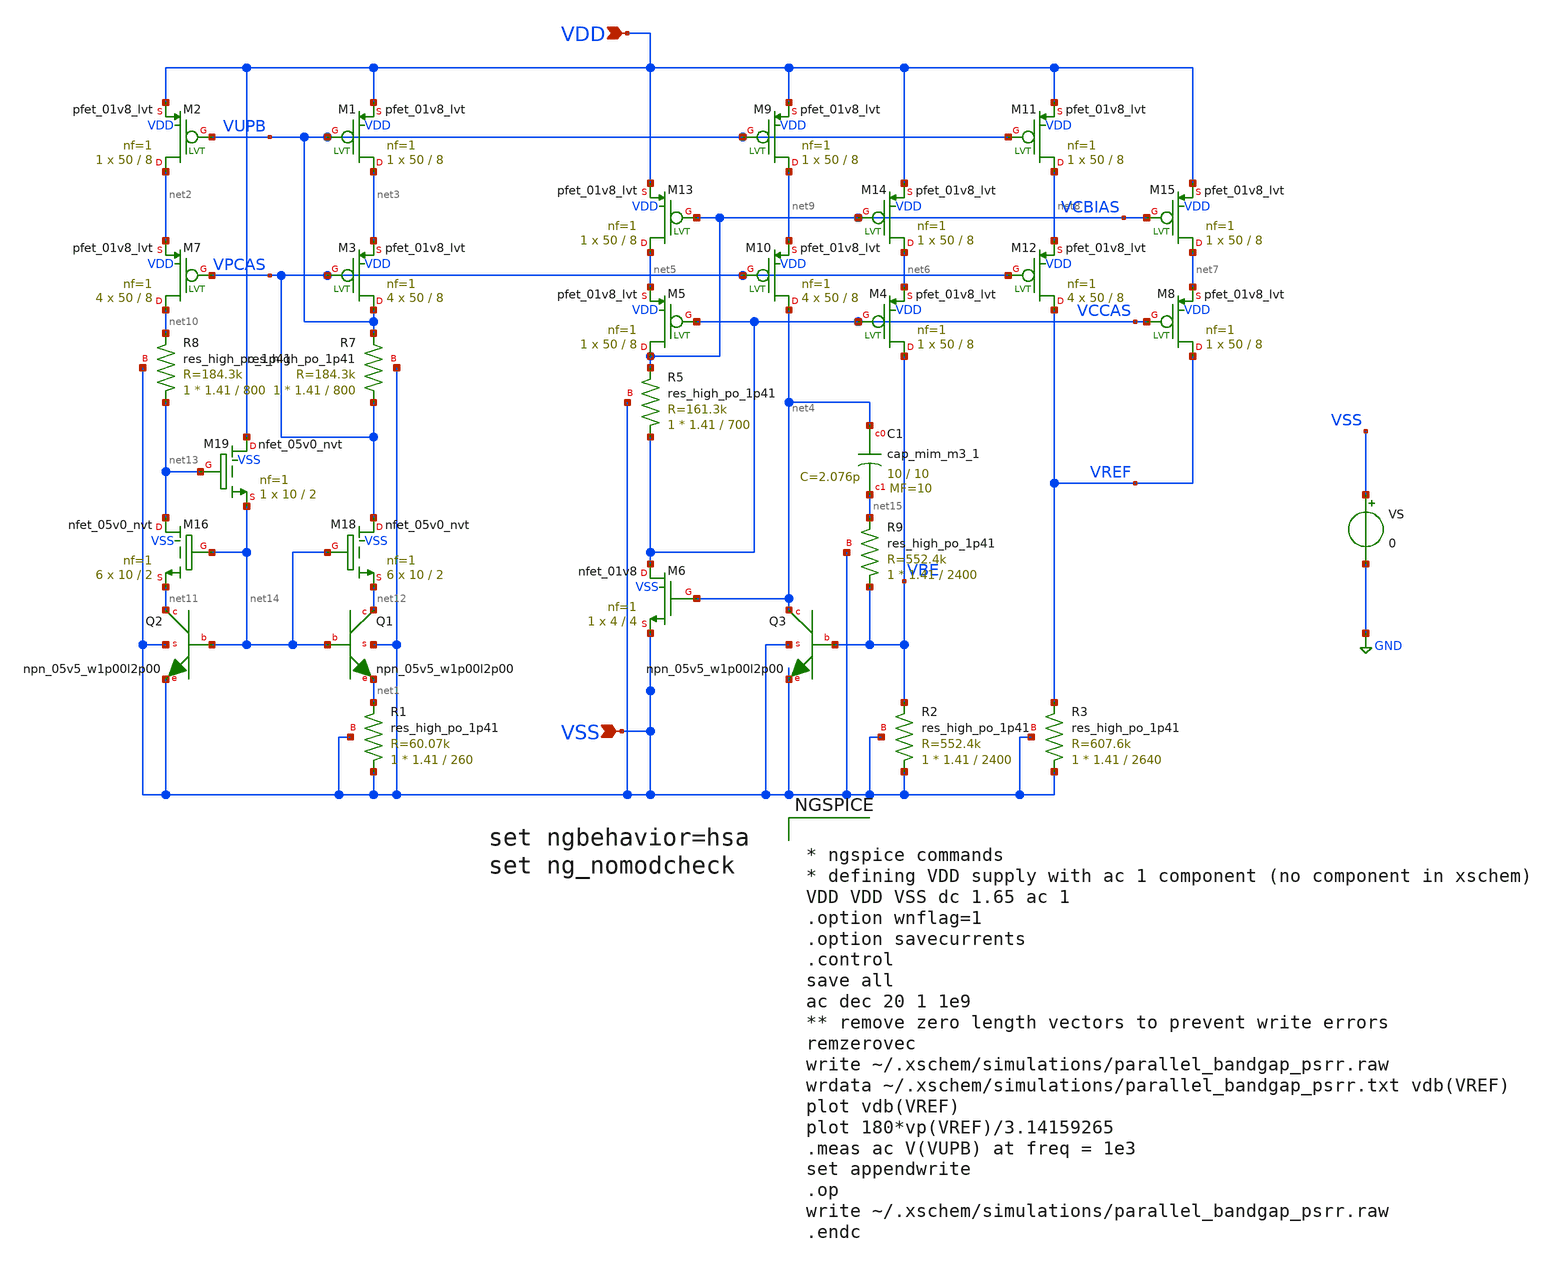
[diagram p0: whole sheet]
** sch_path: designs/parallel_bandgap_psrr.sch
**.subckt parallel_bandgap_psrr VDD VSS
*.ipin VDD
*.ipin VSS
XM1 net3 VUPB VDD VDD sky130_fd_pr__pfet_01v8_lvt L=8 W=50 nf=1 ad='int((nf+1)/2) * W/nf * 0.29' as='int((nf+2)/2) * W/nf * 0.29'
+ pd='2*int((nf+1)/2) * (W/nf + 0.29)' ps='2*int((nf+2)/2) * (W/nf + 0.29)' nrd='0.29 / W' nrs='0.29 / W'
+ sa=0 sb=0 sd=0 mult=1 m=1
XM2 net2 VUPB VDD VDD sky130_fd_pr__pfet_01v8_lvt L=8 W=50 nf=1 ad='int((nf+1)/2) * W/nf * 0.29' as='int((nf+2)/2) * W/nf * 0.29'
+ pd='2*int((nf+1)/2) * (W/nf + 0.29)' ps='2*int((nf+2)/2) * (W/nf + 0.29)' nrd='0.29 / W' nrs='0.29 / W'
+ sa=0 sb=0 sd=0 mult=1 m=1
XQ1 net12 net14 net1 VSS sky130_fd_pr__npn_05v5_w1p00l2p00
XQ2 net11 net14 VSS VSS sky130_fd_pr__npn_05v5_w1p00l2p00
XR1 VSS net1 VSS sky130_fd_pr__res_high_po_1p41 L=260 mult=1 m=1
XQ3 net4 VBE VSS VSS sky130_fd_pr__npn_05v5_w1p00l2p00
XR2 VSS VBE VSS sky130_fd_pr__res_high_po_1p41 L=2400 mult=1 m=1
XM4 VBE VCCAS net6 VDD sky130_fd_pr__pfet_01v8_lvt L=8 W=50 nf=1 ad='int((nf+1)/2) * W/nf * 0.29' as='int((nf+2)/2) * W/nf * 0.29'
+ pd='2*int((nf+1)/2) * (W/nf + 0.29)' ps='2*int((nf+2)/2) * (W/nf + 0.29)' nrd='0.29 / W' nrs='0.29 / W'
+ sa=0 sb=0 sd=0 mult=1 m=1
XM5 VCBIAS VCCAS net5 VDD sky130_fd_pr__pfet_01v8_lvt L=8 W=50 nf=1 ad='int((nf+1)/2) * W/nf * 0.29'
+ as='int((nf+2)/2) * W/nf * 0.29' pd='2*int((nf+1)/2) * (W/nf + 0.29)' ps='2*int((nf+2)/2) * (W/nf + 0.29)'
+ nrd='0.29 / W' nrs='0.29 / W' sa=0 sb=0 sd=0 mult=1 m=1
XM6 VCCAS net4 VSS VSS sky130_fd_pr__nfet_01v8 L=4 W=4 nf=1 ad='int((nf+1)/2) * W/nf * 0.29' as='int((nf+2)/2) * W/nf * 0.29'
+ pd='2*int((nf+1)/2) * (W/nf + 0.29)' ps='2*int((nf+2)/2) * (W/nf + 0.29)' nrd='0.29 / W' nrs='0.29 / W'
+ sa=0 sb=0 sd=0 mult=1 m=1
XR3 VSS VREF VSS sky130_fd_pr__res_high_po_1p41 L=2640 mult=1 m=1
XM8 VREF VCCAS net7 VDD sky130_fd_pr__pfet_01v8_lvt L=8 W=50 nf=1 ad='int((nf+1)/2) * W/nf * 0.29' as='int((nf+2)/2) * W/nf * 0.29'
+ pd='2*int((nf+1)/2) * (W/nf + 0.29)' ps='2*int((nf+2)/2) * (W/nf + 0.29)' nrd='0.29 / W' nrs='0.29 / W'
+ sa=0 sb=0 sd=0 mult=1 m=1
XM3 VUPB VPCAS net3 VDD sky130_fd_pr__pfet_01v8_lvt L=8 W=50 nf=1 ad='int((nf+1)/2) * W/nf * 0.29' as='int((nf+2)/2) * W/nf * 0.29'
+ pd='2*int((nf+1)/2) * (W/nf + 0.29)' ps='2*int((nf+2)/2) * (W/nf + 0.29)' nrd='0.29 / W' nrs='0.29 / W'
+ sa=0 sb=0 sd=0 mult=4 m=4
XM7 net10 VPCAS net2 VDD sky130_fd_pr__pfet_01v8_lvt L=8 W=50 nf=1 ad='int((nf+1)/2) * W/nf * 0.29' as='int((nf+2)/2) * W/nf * 0.29'
+ pd='2*int((nf+1)/2) * (W/nf + 0.29)' ps='2*int((nf+2)/2) * (W/nf + 0.29)' nrd='0.29 / W' nrs='0.29 / W'
+ sa=0 sb=0 sd=0 mult=4 m=4
XM9 net9 VUPB VDD VDD sky130_fd_pr__pfet_01v8_lvt L=8 W=50 nf=1 ad='int((nf+1)/2) * W/nf * 0.29' as='int((nf+2)/2) * W/nf * 0.29'
+ pd='2*int((nf+1)/2) * (W/nf + 0.29)' ps='2*int((nf+2)/2) * (W/nf + 0.29)' nrd='0.29 / W' nrs='0.29 / W'
+ sa=0 sb=0 sd=0 mult=1 m=1
XM10 net4 VPCAS net9 VDD sky130_fd_pr__pfet_01v8_lvt L=8 W=50 nf=1 ad='int((nf+1)/2) * W/nf * 0.29' as='int((nf+2)/2) * W/nf * 0.29'
+ pd='2*int((nf+1)/2) * (W/nf + 0.29)' ps='2*int((nf+2)/2) * (W/nf + 0.29)' nrd='0.29 / W' nrs='0.29 / W'
+ sa=0 sb=0 sd=0 mult=4 m=4
XM11 net8 VUPB VDD VDD sky130_fd_pr__pfet_01v8_lvt L=8 W=50 nf=1 ad='int((nf+1)/2) * W/nf * 0.29' as='int((nf+2)/2) * W/nf * 0.29'
+ pd='2*int((nf+1)/2) * (W/nf + 0.29)' ps='2*int((nf+2)/2) * (W/nf + 0.29)' nrd='0.29 / W' nrs='0.29 / W'
+ sa=0 sb=0 sd=0 mult=1 m=1
XM12 VREF VPCAS net8 VDD sky130_fd_pr__pfet_01v8_lvt L=8 W=50 nf=1 ad='int((nf+1)/2) * W/nf * 0.29' as='int((nf+2)/2) * W/nf * 0.29'
+ pd='2*int((nf+1)/2) * (W/nf + 0.29)' ps='2*int((nf+2)/2) * (W/nf + 0.29)' nrd='0.29 / W' nrs='0.29 / W'
+ sa=0 sb=0 sd=0 mult=4 m=4
XM13 net5 VCBIAS VDD VDD sky130_fd_pr__pfet_01v8_lvt L=8 W=50 nf=1 ad='int((nf+1)/2) * W/nf * 0.29' as='int((nf+2)/2) * W/nf * 0.29'
+ pd='2*int((nf+1)/2) * (W/nf + 0.29)' ps='2*int((nf+2)/2) * (W/nf + 0.29)' nrd='0.29 / W' nrs='0.29 / W'
+ sa=0 sb=0 sd=0 mult=1 m=1
XM14 net6 VCBIAS VDD VDD sky130_fd_pr__pfet_01v8_lvt L=8 W=50 nf=1 ad='int((nf+1)/2) * W/nf * 0.29' as='int((nf+2)/2) * W/nf * 0.29'
+ pd='2*int((nf+1)/2) * (W/nf + 0.29)' ps='2*int((nf+2)/2) * (W/nf + 0.29)' nrd='0.29 / W' nrs='0.29 / W'
+ sa=0 sb=0 sd=0 mult=1 m=1
XR5 VCCAS VCBIAS VSS sky130_fd_pr__res_high_po_1p41 L=700 mult=1 m=1
XM15 net7 VCBIAS VDD VDD sky130_fd_pr__pfet_01v8_lvt L=8 W=50 nf=1 ad='int((nf+1)/2) * W/nf * 0.29' as='int((nf+2)/2) * W/nf * 0.29'
+ pd='2*int((nf+1)/2) * (W/nf + 0.29)' ps='2*int((nf+2)/2) * (W/nf + 0.29)' nrd='0.29 / W' nrs='0.29 / W'
+ sa=0 sb=0 sd=0 mult=1 m=1
VS VSS GND 0
XR7 VPCAS VUPB VSS sky130_fd_pr__res_high_po_1p41 L=800 mult=1 m=1
XR8 net13 net10 VSS sky130_fd_pr__res_high_po_1p41 L=800 mult=1 m=1
XM16 net13 net14 net11 VSS sky130_fd_pr__nfet_05v0_nvt L=2 W=10 nf=1 ad='int((nf+1)/2) * W/nf * 0.29'
+ as='int((nf+2)/2) * W/nf * 0.29' pd='2*int((nf+1)/2) * (W/nf + 0.29)' ps='2*int((nf+2)/2) * (W/nf + 0.29)'
+ nrd='0.29 / W' nrs='0.29 / W' sa=0 sb=0 sd=0 mult=6 m=6
XM18 VPCAS net14 net12 VSS sky130_fd_pr__nfet_05v0_nvt L=2 W=10 nf=1 ad='int((nf+1)/2) * W/nf * 0.29'
+ as='int((nf+2)/2) * W/nf * 0.29' pd='2*int((nf+1)/2) * (W/nf + 0.29)' ps='2*int((nf+2)/2) * (W/nf + 0.29)'
+ nrd='0.29 / W' nrs='0.29 / W' sa=0 sb=0 sd=0 mult=6 m=6
XM19 VDD net13 net14 VSS sky130_fd_pr__nfet_05v0_nvt L=2 W=10 nf=1 ad='int((nf+1)/2) * W/nf * 0.29' as='int((nf+2)/2) * W/nf * 0.29'
+ pd='2*int((nf+1)/2) * (W/nf + 0.29)' ps='2*int((nf+2)/2) * (W/nf + 0.29)' nrd='0.29 / W' nrs='0.29 / W'
+ sa=0 sb=0 sd=0 mult=1 m=1
XR9 VBE net15 VSS sky130_fd_pr__res_high_po_1p41 L=2400 mult=1 m=1
XC1 net4 net15 sky130_fd_pr__cap_mim_m3_1 W=10 L=10 MF=10 m=10
**** begin user architecture code


* ngspice commands
* defining VDD supply with ac 1 component (no component in xschem)
VDD VDD VSS dc 1.65 ac 1
.option wnflag=1
.option savecurrents
.control
save all
ac dec 20 1 1e9
** remove zero length vectors to prevent write errors
remzerovec
write ~/.xschem/simulations/parallel_bandgap_psrr.raw
wrdata ~/.xschem/simulations/parallel_bandgap_psrr.txt vdb(VREF)
plot vdb(VREF)
plot 180*vp(VREF)/3.14159265
.meas ac V(VUPB) at freq = 1e3
set appendwrite
.op
write ~/.xschem/simulations/parallel_bandgap_psrr.raw
.endc



** opencircuitdesign pdks install
.lib /foss/pdks/sky130A/libs.tech/combined/sky130.corners.lib.spice tt

**** end user architecture code
**.ends
.GLOBAL GND
.end
